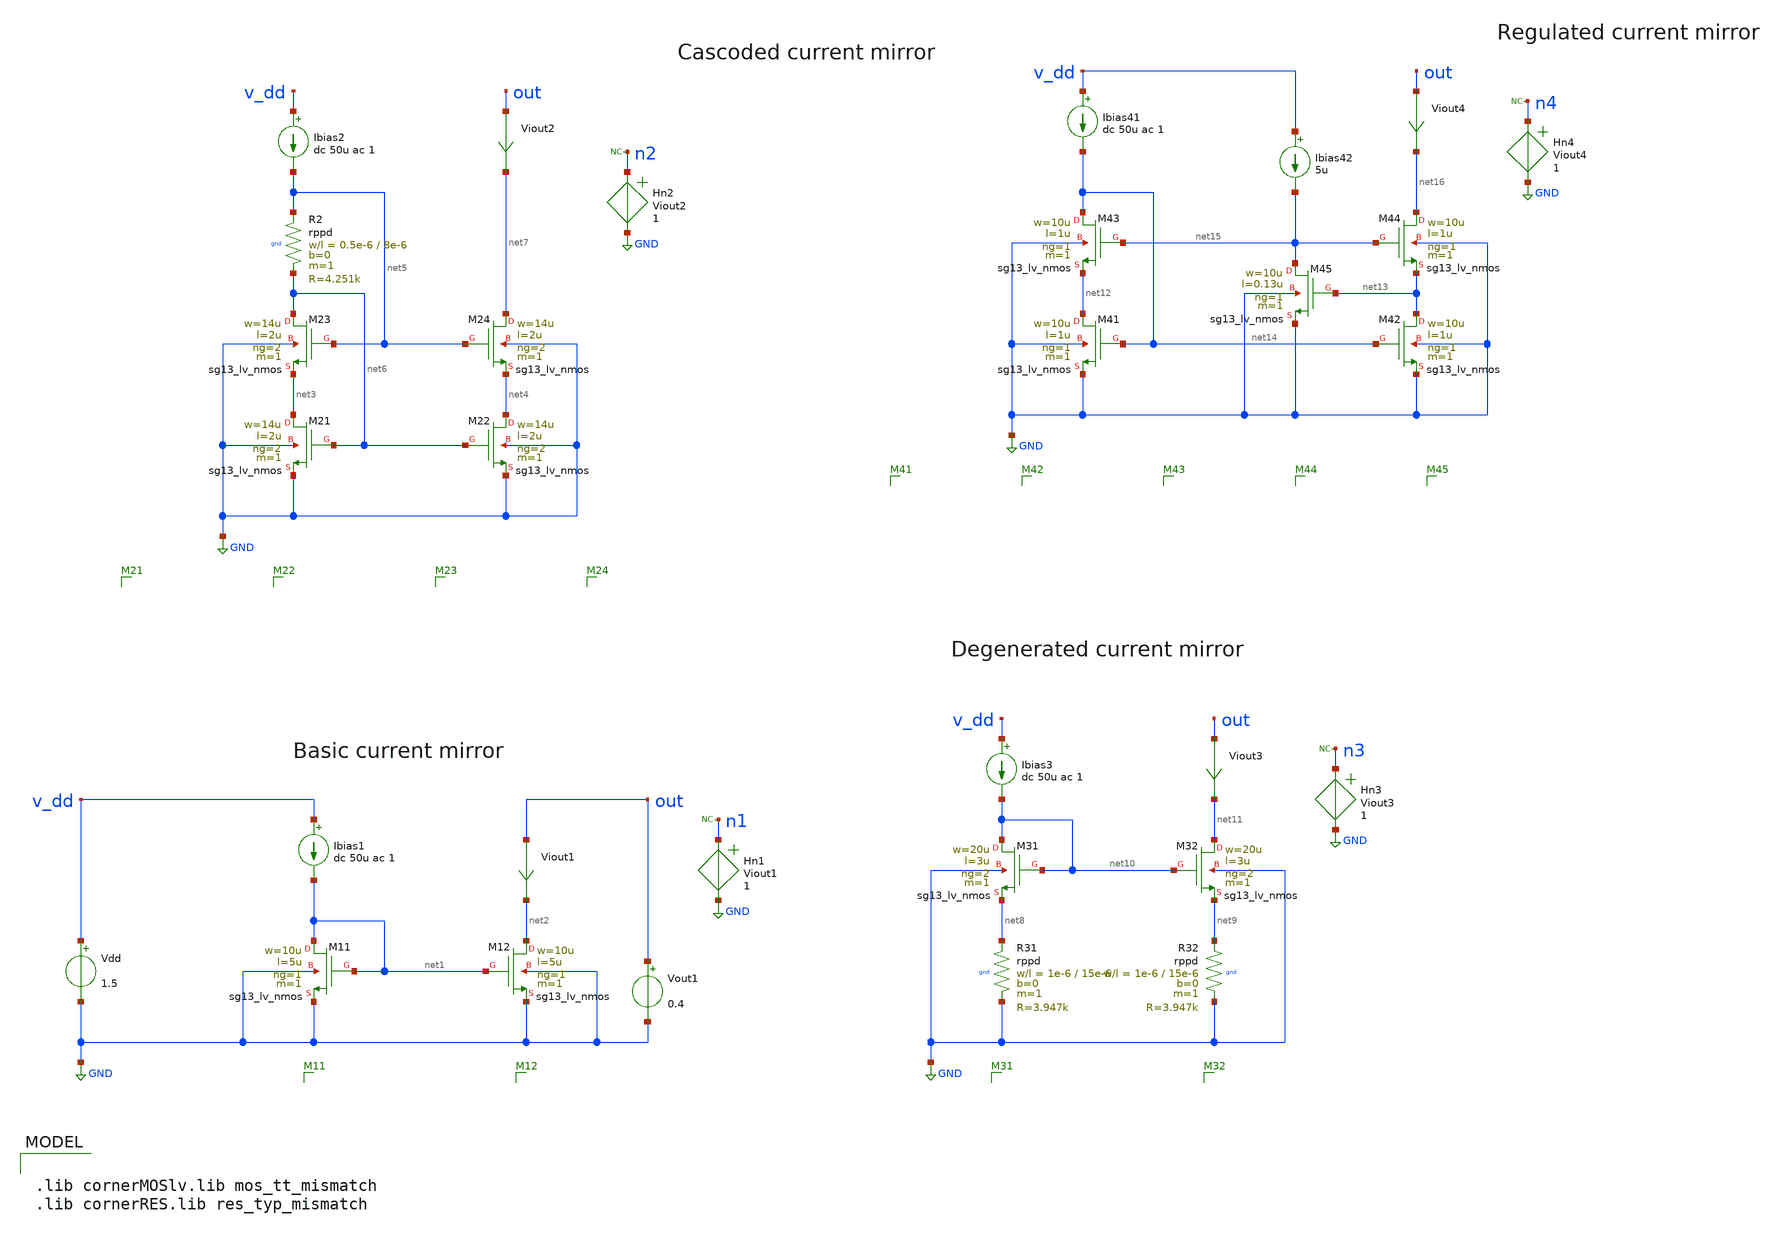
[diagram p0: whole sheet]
** sch_path: xschem/current_mirror_variations.sch
* (c) 2025 Harald Pretl, Apache-2.0 license
**.subckt current_mirror_variations
Vdd v_dd GND 1.5
XM11 net1 net1 GND GND sg13_lv_nmos w=10u l=5u ng=1 m=1 mm_ok=1
Ibias1 v_dd net1 dc 50u ac 1
XM12 net2 net1 GND GND sg13_lv_nmos w=10u l=5u ng=1 m=1 mm_ok=1
Vout1 out GND 0.4
Viout1 out net2 0
.save i(viout1)
XM21 net3 net6 GND GND sg13_lv_nmos w=14u l=2u ng=2 m=1 mm_ok=1
Ibias2 v_dd net5 dc 50u ac 1
XM22 net4 net6 GND GND sg13_lv_nmos w=14u l=2u ng=2 m=1 mm_ok=1
Viout2 out net7 0
.save i(viout2)
XM23 net6 net5 net3 GND sg13_lv_nmos w=14u l=2u ng=2 m=1 mm_ok=1
XM24 net7 net5 net4 GND sg13_lv_nmos w=14u l=2u ng=2 m=1 mm_ok=1
Ibias3 v_dd net10 dc 50u ac 1
Viout3 out net11 0
.save i(viout3)
XM31 net10 net10 net8 GND sg13_lv_nmos w=20u l=3u ng=2 m=1 mm_ok=1
XM32 net11 net10 net9 GND sg13_lv_nmos w=20u l=3u ng=2 m=1 mm_ok=1
XM41 net12 net14 GND GND sg13_lv_nmos w=10u l=1u ng=1 m=1 mm_ok=1
Ibias41 v_dd net14 dc 50u ac 1
XM42 net13 net14 GND GND sg13_lv_nmos w=10u l=1u ng=1 m=1 mm_ok=1
Viout4 out net16 0
.save i(viout4)
XM43 net14 net15 net12 GND sg13_lv_nmos w=10u l=1u ng=1 m=1 mm_ok=1
XM44 net16 net15 net13 GND sg13_lv_nmos w=10u l=1u ng=1 m=1 mm_ok=1
XM45 net15 net13 GND GND sg13_lv_nmos w=10u l=0.13u ng=1 m=1 mm_ok=1
Ibias42 v_dd net15 5u
XR2 net5 net6 gnd rppd w=0.5e-6 l=8e-6 m=1 b=0 mm_ok=1
XR31 net8 GND gnd rppd w=1e-6 l=15e-6 m=1 b=0 mm_ok=1
XR32 net9 GND gnd rppd w=1e-6 l=15e-6 m=1 b=0 mm_ok=1
Hn1 n1 GND Viout1 1
* noconn n1
Hn2 n2 GND Viout2 1
* noconn n2
Hn3 n3 GND Viout3 1
* noconn n3
Hn4 n4 GND Viout4 1
* noconn n4
**** begin user architecture code

.lib cornerMOSlv.lib mos_tt_mismatch
.lib cornerRES.lib res_typ_mismatch



.temp 27
.include current_mirror_variations.save
.control
option noacct noinit seed=1
save all

let mcruns = 500
let runs = 0

*
* Simulate dc output characteristics
*
op
write current_mirror_variations.raw
dc Vout1 0 1.5 10m
plot i(Viout1) i(viout2) i(viout3) i(viout4)
wrdata curmir_variations.txt i(viout1) i(viout2) i(viout3) i(viout4)

*
* Simulate output noise
*
noise v(n1) ibias1 dec 100 1MEG 100MEG
setplot noise1
wrdata curmir_variations_noise1.txt onoise_spectrum

noise v(n2) ibias2 dec 100 1MEG 100MEG
setplot noise3
wrdata curmir_variations_noise2.txt onoise_spectrum

noise v(n3) ibias3 dec 100 1MEG 100MEG
setplot noise5
wrdata curmir_variations_noise3.txt onoise_spectrum

noise v(n4) ibias41 dec 100 1MEG 100MEG
setplot noise7
wrdata curmir_variations_noise4.txt onoise_spectrum

*
* Simulate mismatch of output current
*
shell rm curmir_variations_mc1.txt
shell rm curmir_variations_mc2.txt
shell rm curmir_variations_mc3.txt
shell rm curmir_variations_mc4.txt
dowhile runs < mcruns
  reset
  option noacct noinit seed=1
  let runs = runs + 1
  op
  print i(Viout1) >> curmir_variations_mc1.txt
  print i(Viout2) >> curmir_variations_mc2.txt
  print i(Viout3) >> curmir_variations_mc3.txt
  print i(Viout4) >> curmir_variations_mc4.txt
end

.endc


**** end user architecture code
**.ends
.GLOBAL GND
.end
